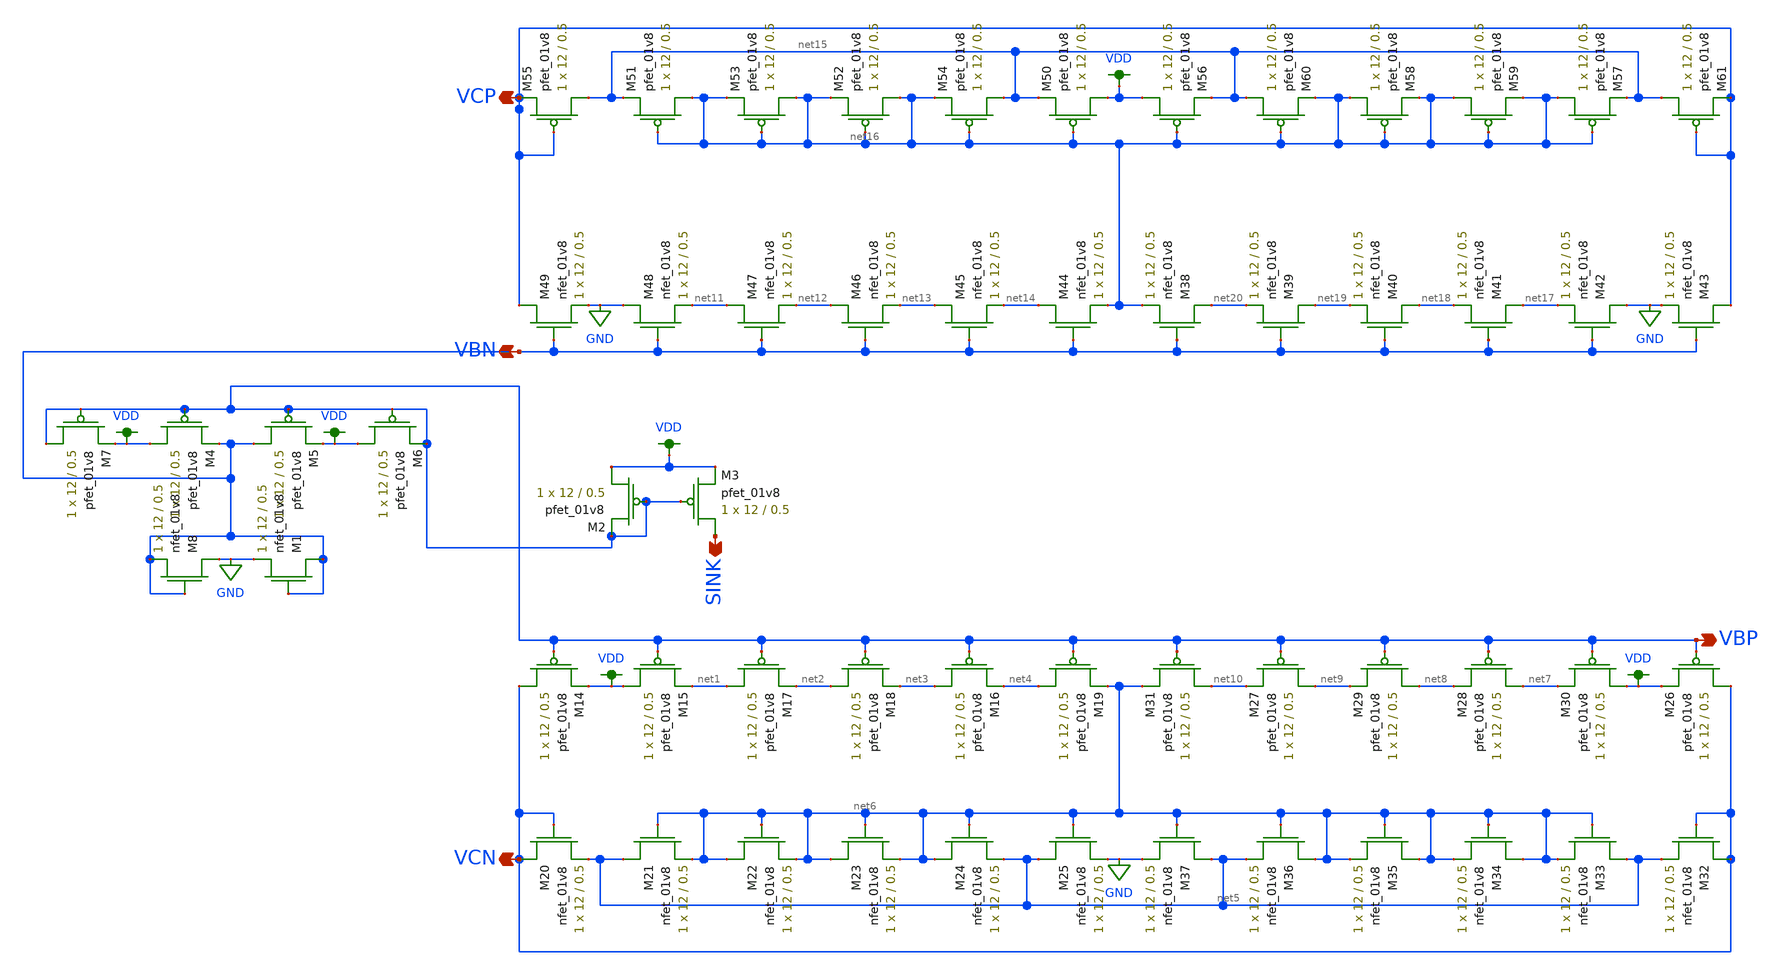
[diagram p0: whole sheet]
** sch_path: schemas/BiasGen.sch
**.subckt BiasGen VBP VCN VCP VBN SINK
*.opin VBP
*.opin VCN
*.opin VCP
*.opin VBN
*.opin SINK
XM14 VCN VBP VDD VDD sky130_fd_pr__pfet_01v8 L=0.5 W=12 nf=1 ad='int((nf+1)/2) * W/nf * 0.29' as='int((nf+2)/2) * W/nf * 0.29'
+ pd='2*int((nf+1)/2) * (W/nf + 0.29)' ps='2*int((nf+2)/2) * (W/nf + 0.29)' nrd='0.29 / W' nrs='0.29 / W'
+ sa=0 sb=0 sd=0 mult=1 m=1
XM16 net3 VBP net4 VDD sky130_fd_pr__pfet_01v8 L=0.5 W=12 nf=1 ad='int((nf+1)/2) * W/nf * 0.29' as='int((nf+2)/2) * W/nf * 0.29'
+ pd='2*int((nf+1)/2) * (W/nf + 0.29)' ps='2*int((nf+2)/2) * (W/nf + 0.29)' nrd='0.29 / W' nrs='0.29 / W'
+ sa=0 sb=0 sd=0 mult=1 m=1
XM17 net1 VBP net2 VDD sky130_fd_pr__pfet_01v8 L=0.5 W=12 nf=1 ad='int((nf+1)/2) * W/nf * 0.29' as='int((nf+2)/2) * W/nf * 0.29'
+ pd='2*int((nf+1)/2) * (W/nf + 0.29)' ps='2*int((nf+2)/2) * (W/nf + 0.29)' nrd='0.29 / W' nrs='0.29 / W'
+ sa=0 sb=0 sd=0 mult=1 m=1
XM18 net2 VBP net3 VDD sky130_fd_pr__pfet_01v8 L=0.5 W=12 nf=1 ad='int((nf+1)/2) * W/nf * 0.29' as='int((nf+2)/2) * W/nf * 0.29'
+ pd='2*int((nf+1)/2) * (W/nf + 0.29)' ps='2*int((nf+2)/2) * (W/nf + 0.29)' nrd='0.29 / W' nrs='0.29 / W'
+ sa=0 sb=0 sd=0 mult=1 m=1
XM15 VDD VBP net1 VDD sky130_fd_pr__pfet_01v8 L=0.5 W=12 nf=1 ad='int((nf+1)/2) * W/nf * 0.29' as='int((nf+2)/2) * W/nf * 0.29'
+ pd='2*int((nf+1)/2) * (W/nf + 0.29)' ps='2*int((nf+2)/2) * (W/nf + 0.29)' nrd='0.29 / W' nrs='0.29 / W'
+ sa=0 sb=0 sd=0 mult=1 m=1
XM19 net4 VBP net6 VDD sky130_fd_pr__pfet_01v8 L=0.5 W=12 nf=1 ad='int((nf+1)/2) * W/nf * 0.29' as='int((nf+2)/2) * W/nf * 0.29'
+ pd='2*int((nf+1)/2) * (W/nf + 0.29)' ps='2*int((nf+2)/2) * (W/nf + 0.29)' nrd='0.29 / W' nrs='0.29 / W'
+ sa=0 sb=0 sd=0 mult=1 m=1
XM20 VCN VCN net5 GND sky130_fd_pr__nfet_01v8 L=0.5 W=12 nf=1 ad='int((nf+1)/2) * W/nf * 0.29' as='int((nf+2)/2) * W/nf * 0.29'
+ pd='2*int((nf+1)/2) * (W/nf + 0.29)' ps='2*int((nf+2)/2) * (W/nf + 0.29)' nrd='0.29 / W' nrs='0.29 / W'
+ sa=0 sb=0 sd=0 mult=1 m=1
XM21 net5 net6 net6 GND sky130_fd_pr__nfet_01v8 L=0.5 W=12 nf=1 ad='int((nf+1)/2) * W/nf * 0.29' as='int((nf+2)/2) * W/nf * 0.29'
+ pd='2*int((nf+1)/2) * (W/nf + 0.29)' ps='2*int((nf+2)/2) * (W/nf + 0.29)' nrd='0.29 / W' nrs='0.29 / W'
+ sa=0 sb=0 sd=0 mult=1 m=1
XM22 net6 net6 net6 GND sky130_fd_pr__nfet_01v8 L=0.5 W=12 nf=1 ad='int((nf+1)/2) * W/nf * 0.29' as='int((nf+2)/2) * W/nf * 0.29'
+ pd='2*int((nf+1)/2) * (W/nf + 0.29)' ps='2*int((nf+2)/2) * (W/nf + 0.29)' nrd='0.29 / W' nrs='0.29 / W'
+ sa=0 sb=0 sd=0 mult=1 m=1
XM23 net6 net6 net6 GND sky130_fd_pr__nfet_01v8 L=0.5 W=12 nf=1 ad='int((nf+1)/2) * W/nf * 0.29' as='int((nf+2)/2) * W/nf * 0.29'
+ pd='2*int((nf+1)/2) * (W/nf + 0.29)' ps='2*int((nf+2)/2) * (W/nf + 0.29)' nrd='0.29 / W' nrs='0.29 / W'
+ sa=0 sb=0 sd=0 mult=1 m=1
XM24 net6 net6 net5 GND sky130_fd_pr__nfet_01v8 L=0.5 W=12 nf=1 ad='int((nf+1)/2) * W/nf * 0.29' as='int((nf+2)/2) * W/nf * 0.29'
+ pd='2*int((nf+1)/2) * (W/nf + 0.29)' ps='2*int((nf+2)/2) * (W/nf + 0.29)' nrd='0.29 / W' nrs='0.29 / W'
+ sa=0 sb=0 sd=0 mult=1 m=1
XM25 net5 net6 GND GND sky130_fd_pr__nfet_01v8 L=0.5 W=12 nf=1 ad='int((nf+1)/2) * W/nf * 0.29' as='int((nf+2)/2) * W/nf * 0.29'
+ pd='2*int((nf+1)/2) * (W/nf + 0.29)' ps='2*int((nf+2)/2) * (W/nf + 0.29)' nrd='0.29 / W' nrs='0.29 / W'
+ sa=0 sb=0 sd=0 mult=1 m=1
XM26 VCN VBP VDD VDD sky130_fd_pr__pfet_01v8 L=0.5 W=12 nf=1 ad='int((nf+1)/2) * W/nf * 0.29' as='int((nf+2)/2) * W/nf * 0.29'
+ pd='2*int((nf+1)/2) * (W/nf + 0.29)' ps='2*int((nf+2)/2) * (W/nf + 0.29)' nrd='0.29 / W' nrs='0.29 / W'
+ sa=0 sb=0 sd=0 mult=1 m=1
XM27 net9 VBP net10 VDD sky130_fd_pr__pfet_01v8 L=0.5 W=12 nf=1 ad='int((nf+1)/2) * W/nf * 0.29' as='int((nf+2)/2) * W/nf * 0.29'
+ pd='2*int((nf+1)/2) * (W/nf + 0.29)' ps='2*int((nf+2)/2) * (W/nf + 0.29)' nrd='0.29 / W' nrs='0.29 / W'
+ sa=0 sb=0 sd=0 mult=1 m=1
XM28 net7 VBP net8 VDD sky130_fd_pr__pfet_01v8 L=0.5 W=12 nf=1 ad='int((nf+1)/2) * W/nf * 0.29' as='int((nf+2)/2) * W/nf * 0.29'
+ pd='2*int((nf+1)/2) * (W/nf + 0.29)' ps='2*int((nf+2)/2) * (W/nf + 0.29)' nrd='0.29 / W' nrs='0.29 / W'
+ sa=0 sb=0 sd=0 mult=1 m=1
XM29 net8 VBP net9 VDD sky130_fd_pr__pfet_01v8 L=0.5 W=12 nf=1 ad='int((nf+1)/2) * W/nf * 0.29' as='int((nf+2)/2) * W/nf * 0.29'
+ pd='2*int((nf+1)/2) * (W/nf + 0.29)' ps='2*int((nf+2)/2) * (W/nf + 0.29)' nrd='0.29 / W' nrs='0.29 / W'
+ sa=0 sb=0 sd=0 mult=1 m=1
XM30 VDD VBP net7 VDD sky130_fd_pr__pfet_01v8 L=0.5 W=12 nf=1 ad='int((nf+1)/2) * W/nf * 0.29' as='int((nf+2)/2) * W/nf * 0.29'
+ pd='2*int((nf+1)/2) * (W/nf + 0.29)' ps='2*int((nf+2)/2) * (W/nf + 0.29)' nrd='0.29 / W' nrs='0.29 / W'
+ sa=0 sb=0 sd=0 mult=1 m=1
XM31 net10 VBP net6 VDD sky130_fd_pr__pfet_01v8 L=0.5 W=12 nf=1 ad='int((nf+1)/2) * W/nf * 0.29' as='int((nf+2)/2) * W/nf * 0.29'
+ pd='2*int((nf+1)/2) * (W/nf + 0.29)' ps='2*int((nf+2)/2) * (W/nf + 0.29)' nrd='0.29 / W' nrs='0.29 / W'
+ sa=0 sb=0 sd=0 mult=1 m=1
XM32 VCN VCN net5 GND sky130_fd_pr__nfet_01v8 L=0.5 W=12 nf=1 ad='int((nf+1)/2) * W/nf * 0.29' as='int((nf+2)/2) * W/nf * 0.29'
+ pd='2*int((nf+1)/2) * (W/nf + 0.29)' ps='2*int((nf+2)/2) * (W/nf + 0.29)' nrd='0.29 / W' nrs='0.29 / W'
+ sa=0 sb=0 sd=0 mult=1 m=1
XM33 net5 net6 net6 GND sky130_fd_pr__nfet_01v8 L=0.5 W=12 nf=1 ad='int((nf+1)/2) * W/nf * 0.29' as='int((nf+2)/2) * W/nf * 0.29'
+ pd='2*int((nf+1)/2) * (W/nf + 0.29)' ps='2*int((nf+2)/2) * (W/nf + 0.29)' nrd='0.29 / W' nrs='0.29 / W'
+ sa=0 sb=0 sd=0 mult=1 m=1
XM34 net6 net6 net6 GND sky130_fd_pr__nfet_01v8 L=0.5 W=12 nf=1 ad='int((nf+1)/2) * W/nf * 0.29' as='int((nf+2)/2) * W/nf * 0.29'
+ pd='2*int((nf+1)/2) * (W/nf + 0.29)' ps='2*int((nf+2)/2) * (W/nf + 0.29)' nrd='0.29 / W' nrs='0.29 / W'
+ sa=0 sb=0 sd=0 mult=1 m=1
XM35 net6 net6 net6 GND sky130_fd_pr__nfet_01v8 L=0.5 W=12 nf=1 ad='int((nf+1)/2) * W/nf * 0.29' as='int((nf+2)/2) * W/nf * 0.29'
+ pd='2*int((nf+1)/2) * (W/nf + 0.29)' ps='2*int((nf+2)/2) * (W/nf + 0.29)' nrd='0.29 / W' nrs='0.29 / W'
+ sa=0 sb=0 sd=0 mult=1 m=1
XM36 net6 net6 net5 GND sky130_fd_pr__nfet_01v8 L=0.5 W=12 nf=1 ad='int((nf+1)/2) * W/nf * 0.29' as='int((nf+2)/2) * W/nf * 0.29'
+ pd='2*int((nf+1)/2) * (W/nf + 0.29)' ps='2*int((nf+2)/2) * (W/nf + 0.29)' nrd='0.29 / W' nrs='0.29 / W'
+ sa=0 sb=0 sd=0 mult=1 m=1
XM37 net5 net6 GND GND sky130_fd_pr__nfet_01v8 L=0.5 W=12 nf=1 ad='int((nf+1)/2) * W/nf * 0.29' as='int((nf+2)/2) * W/nf * 0.29'
+ pd='2*int((nf+1)/2) * (W/nf + 0.29)' ps='2*int((nf+2)/2) * (W/nf + 0.29)' nrd='0.29 / W' nrs='0.29 / W'
+ sa=0 sb=0 sd=0 mult=1 m=1
XM44 net14 VBN net16 GND sky130_fd_pr__nfet_01v8 L=0.5 W=12 nf=1 ad='int((nf+1)/2) * W/nf * 0.29' as='int((nf+2)/2) * W/nf * 0.29'
+ pd='2*int((nf+1)/2) * (W/nf + 0.29)' ps='2*int((nf+2)/2) * (W/nf + 0.29)' nrd='0.29 / W' nrs='0.29 / W'
+ sa=0 sb=0 sd=0 mult=1 m=1
XM45 net13 VBN net14 GND sky130_fd_pr__nfet_01v8 L=0.5 W=12 nf=1 ad='int((nf+1)/2) * W/nf * 0.29' as='int((nf+2)/2) * W/nf * 0.29'
+ pd='2*int((nf+1)/2) * (W/nf + 0.29)' ps='2*int((nf+2)/2) * (W/nf + 0.29)' nrd='0.29 / W' nrs='0.29 / W'
+ sa=0 sb=0 sd=0 mult=1 m=1
XM46 net12 VBN net13 GND sky130_fd_pr__nfet_01v8 L=0.5 W=12 nf=1 ad='int((nf+1)/2) * W/nf * 0.29' as='int((nf+2)/2) * W/nf * 0.29'
+ pd='2*int((nf+1)/2) * (W/nf + 0.29)' ps='2*int((nf+2)/2) * (W/nf + 0.29)' nrd='0.29 / W' nrs='0.29 / W'
+ sa=0 sb=0 sd=0 mult=1 m=1
XM47 net11 VBN net12 GND sky130_fd_pr__nfet_01v8 L=0.5 W=12 nf=1 ad='int((nf+1)/2) * W/nf * 0.29' as='int((nf+2)/2) * W/nf * 0.29'
+ pd='2*int((nf+1)/2) * (W/nf + 0.29)' ps='2*int((nf+2)/2) * (W/nf + 0.29)' nrd='0.29 / W' nrs='0.29 / W'
+ sa=0 sb=0 sd=0 mult=1 m=1
XM48 GND VBN net11 GND sky130_fd_pr__nfet_01v8 L=0.5 W=12 nf=1 ad='int((nf+1)/2) * W/nf * 0.29' as='int((nf+2)/2) * W/nf * 0.29'
+ pd='2*int((nf+1)/2) * (W/nf + 0.29)' ps='2*int((nf+2)/2) * (W/nf + 0.29)' nrd='0.29 / W' nrs='0.29 / W'
+ sa=0 sb=0 sd=0 mult=1 m=1
XM49 VCP VBN GND GND sky130_fd_pr__nfet_01v8 L=0.5 W=12 nf=1 ad='int((nf+1)/2) * W/nf * 0.29' as='int((nf+2)/2) * W/nf * 0.29'
+ pd='2*int((nf+1)/2) * (W/nf + 0.29)' ps='2*int((nf+2)/2) * (W/nf + 0.29)' nrd='0.29 / W' nrs='0.29 / W'
+ sa=0 sb=0 sd=0 mult=1 m=1
XM50 VDD net16 net15 VDD sky130_fd_pr__pfet_01v8 L=0.5 W=12 nf=1 ad='int((nf+1)/2) * W/nf * 0.29' as='int((nf+2)/2) * W/nf * 0.29'
+ pd='2*int((nf+1)/2) * (W/nf + 0.29)' ps='2*int((nf+2)/2) * (W/nf + 0.29)' nrd='0.29 / W' nrs='0.29 / W'
+ sa=0 sb=0 sd=0 mult=1 m=1
XM51 net16 net16 net15 VDD sky130_fd_pr__pfet_01v8 L=0.5 W=12 nf=1 ad='int((nf+1)/2) * W/nf * 0.29' as='int((nf+2)/2) * W/nf * 0.29'
+ pd='2*int((nf+1)/2) * (W/nf + 0.29)' ps='2*int((nf+2)/2) * (W/nf + 0.29)' nrd='0.29 / W' nrs='0.29 / W'
+ sa=0 sb=0 sd=0 mult=1 m=1
XM52 net16 net16 net16 VDD sky130_fd_pr__pfet_01v8 L=0.5 W=12 nf=1 ad='int((nf+1)/2) * W/nf * 0.29' as='int((nf+2)/2) * W/nf * 0.29'
+ pd='2*int((nf+1)/2) * (W/nf + 0.29)' ps='2*int((nf+2)/2) * (W/nf + 0.29)' nrd='0.29 / W' nrs='0.29 / W'
+ sa=0 sb=0 sd=0 mult=1 m=1
XM53 net16 net16 net16 VDD sky130_fd_pr__pfet_01v8 L=0.5 W=12 nf=1 ad='int((nf+1)/2) * W/nf * 0.29' as='int((nf+2)/2) * W/nf * 0.29'
+ pd='2*int((nf+1)/2) * (W/nf + 0.29)' ps='2*int((nf+2)/2) * (W/nf + 0.29)' nrd='0.29 / W' nrs='0.29 / W'
+ sa=0 sb=0 sd=0 mult=1 m=1
XM54 net15 net16 net16 VDD sky130_fd_pr__pfet_01v8 L=0.5 W=12 nf=1 ad='int((nf+1)/2) * W/nf * 0.29' as='int((nf+2)/2) * W/nf * 0.29'
+ pd='2*int((nf+1)/2) * (W/nf + 0.29)' ps='2*int((nf+2)/2) * (W/nf + 0.29)' nrd='0.29 / W' nrs='0.29 / W'
+ sa=0 sb=0 sd=0 mult=1 m=1
XM55 net15 VCP VCP VDD sky130_fd_pr__pfet_01v8 L=0.5 W=12 nf=1 ad='int((nf+1)/2) * W/nf * 0.29' as='int((nf+2)/2) * W/nf * 0.29'
+ pd='2*int((nf+1)/2) * (W/nf + 0.29)' ps='2*int((nf+2)/2) * (W/nf + 0.29)' nrd='0.29 / W' nrs='0.29 / W'
+ sa=0 sb=0 sd=0 mult=1 m=1
XM38 net20 VBN net16 GND sky130_fd_pr__nfet_01v8 L=0.5 W=12 nf=1 ad='int((nf+1)/2) * W/nf * 0.29' as='int((nf+2)/2) * W/nf * 0.29'
+ pd='2*int((nf+1)/2) * (W/nf + 0.29)' ps='2*int((nf+2)/2) * (W/nf + 0.29)' nrd='0.29 / W' nrs='0.29 / W'
+ sa=0 sb=0 sd=0 mult=1 m=1
XM39 net19 VBN net20 GND sky130_fd_pr__nfet_01v8 L=0.5 W=12 nf=1 ad='int((nf+1)/2) * W/nf * 0.29' as='int((nf+2)/2) * W/nf * 0.29'
+ pd='2*int((nf+1)/2) * (W/nf + 0.29)' ps='2*int((nf+2)/2) * (W/nf + 0.29)' nrd='0.29 / W' nrs='0.29 / W'
+ sa=0 sb=0 sd=0 mult=1 m=1
XM40 net18 VBN net19 GND sky130_fd_pr__nfet_01v8 L=0.5 W=12 nf=1 ad='int((nf+1)/2) * W/nf * 0.29' as='int((nf+2)/2) * W/nf * 0.29'
+ pd='2*int((nf+1)/2) * (W/nf + 0.29)' ps='2*int((nf+2)/2) * (W/nf + 0.29)' nrd='0.29 / W' nrs='0.29 / W'
+ sa=0 sb=0 sd=0 mult=1 m=1
XM41 net17 VBN net18 GND sky130_fd_pr__nfet_01v8 L=0.5 W=12 nf=1 ad='int((nf+1)/2) * W/nf * 0.29' as='int((nf+2)/2) * W/nf * 0.29'
+ pd='2*int((nf+1)/2) * (W/nf + 0.29)' ps='2*int((nf+2)/2) * (W/nf + 0.29)' nrd='0.29 / W' nrs='0.29 / W'
+ sa=0 sb=0 sd=0 mult=1 m=1
XM42 GND VBN net17 GND sky130_fd_pr__nfet_01v8 L=0.5 W=12 nf=1 ad='int((nf+1)/2) * W/nf * 0.29' as='int((nf+2)/2) * W/nf * 0.29'
+ pd='2*int((nf+1)/2) * (W/nf + 0.29)' ps='2*int((nf+2)/2) * (W/nf + 0.29)' nrd='0.29 / W' nrs='0.29 / W'
+ sa=0 sb=0 sd=0 mult=1 m=1
XM43 VCP VBN GND GND sky130_fd_pr__nfet_01v8 L=0.5 W=12 nf=1 ad='int((nf+1)/2) * W/nf * 0.29' as='int((nf+2)/2) * W/nf * 0.29'
+ pd='2*int((nf+1)/2) * (W/nf + 0.29)' ps='2*int((nf+2)/2) * (W/nf + 0.29)' nrd='0.29 / W' nrs='0.29 / W'
+ sa=0 sb=0 sd=0 mult=1 m=1
XM56 VDD net16 net15 VDD sky130_fd_pr__pfet_01v8 L=0.5 W=12 nf=1 ad='int((nf+1)/2) * W/nf * 0.29' as='int((nf+2)/2) * W/nf * 0.29'
+ pd='2*int((nf+1)/2) * (W/nf + 0.29)' ps='2*int((nf+2)/2) * (W/nf + 0.29)' nrd='0.29 / W' nrs='0.29 / W'
+ sa=0 sb=0 sd=0 mult=1 m=1
XM57 net16 net16 net15 VDD sky130_fd_pr__pfet_01v8 L=0.5 W=12 nf=1 ad='int((nf+1)/2) * W/nf * 0.29' as='int((nf+2)/2) * W/nf * 0.29'
+ pd='2*int((nf+1)/2) * (W/nf + 0.29)' ps='2*int((nf+2)/2) * (W/nf + 0.29)' nrd='0.29 / W' nrs='0.29 / W'
+ sa=0 sb=0 sd=0 mult=1 m=1
XM58 net16 net16 net16 VDD sky130_fd_pr__pfet_01v8 L=0.5 W=12 nf=1 ad='int((nf+1)/2) * W/nf * 0.29' as='int((nf+2)/2) * W/nf * 0.29'
+ pd='2*int((nf+1)/2) * (W/nf + 0.29)' ps='2*int((nf+2)/2) * (W/nf + 0.29)' nrd='0.29 / W' nrs='0.29 / W'
+ sa=0 sb=0 sd=0 mult=1 m=1
XM59 net16 net16 net16 VDD sky130_fd_pr__pfet_01v8 L=0.5 W=12 nf=1 ad='int((nf+1)/2) * W/nf * 0.29' as='int((nf+2)/2) * W/nf * 0.29'
+ pd='2*int((nf+1)/2) * (W/nf + 0.29)' ps='2*int((nf+2)/2) * (W/nf + 0.29)' nrd='0.29 / W' nrs='0.29 / W'
+ sa=0 sb=0 sd=0 mult=1 m=1
XM60 net15 net16 net16 VDD sky130_fd_pr__pfet_01v8 L=0.5 W=12 nf=1 ad='int((nf+1)/2) * W/nf * 0.29' as='int((nf+2)/2) * W/nf * 0.29'
+ pd='2*int((nf+1)/2) * (W/nf + 0.29)' ps='2*int((nf+2)/2) * (W/nf + 0.29)' nrd='0.29 / W' nrs='0.29 / W'
+ sa=0 sb=0 sd=0 mult=1 m=1
XM61 net15 VCP VCP VDD sky130_fd_pr__pfet_01v8 L=0.5 W=12 nf=1 ad='int((nf+1)/2) * W/nf * 0.29' as='int((nf+2)/2) * W/nf * 0.29'
+ pd='2*int((nf+1)/2) * (W/nf + 0.29)' ps='2*int((nf+2)/2) * (W/nf + 0.29)' nrd='0.29 / W' nrs='0.29 / W'
+ sa=0 sb=0 sd=0 mult=1 m=1
XM4 VDD VBP VBN VDD sky130_fd_pr__pfet_01v8 L=0.5 W=12 nf=1 ad='int((nf+1)/2) * W/nf * 0.29' as='int((nf+2)/2) * W/nf * 0.29'
+ pd='2*int((nf+1)/2) * (W/nf + 0.29)' ps='2*int((nf+2)/2) * (W/nf + 0.29)' nrd='0.29 / W' nrs='0.29 / W'
+ sa=0 sb=0 sd=0 mult=1 m=1
XM5 VBN VBP VDD VDD sky130_fd_pr__pfet_01v8 L=0.5 W=12 nf=1 ad='int((nf+1)/2) * W/nf * 0.29' as='int((nf+2)/2) * W/nf * 0.29'
+ pd='2*int((nf+1)/2) * (W/nf + 0.29)' ps='2*int((nf+2)/2) * (W/nf + 0.29)' nrd='0.29 / W' nrs='0.29 / W'
+ sa=0 sb=0 sd=0 mult=1 m=1
XM6 VDD VBP VBP VDD sky130_fd_pr__pfet_01v8 L=0.5 W=12 nf=1 ad='int((nf+1)/2) * W/nf * 0.29' as='int((nf+2)/2) * W/nf * 0.29'
+ pd='2*int((nf+1)/2) * (W/nf + 0.29)' ps='2*int((nf+2)/2) * (W/nf + 0.29)' nrd='0.29 / W' nrs='0.29 / W'
+ sa=0 sb=0 sd=0 mult=1 m=1
XM7 VBP VBP VDD VDD sky130_fd_pr__pfet_01v8 L=0.5 W=12 nf=1 ad='int((nf+1)/2) * W/nf * 0.29' as='int((nf+2)/2) * W/nf * 0.29'
+ pd='2*int((nf+1)/2) * (W/nf + 0.29)' ps='2*int((nf+2)/2) * (W/nf + 0.29)' nrd='0.29 / W' nrs='0.29 / W'
+ sa=0 sb=0 sd=0 mult=1 m=1
XM1 VBN VBN GND GND sky130_fd_pr__nfet_01v8 L=0.5 W=12 nf=1 ad='int((nf+1)/2) * W/nf * 0.29' as='int((nf+2)/2) * W/nf * 0.29'
+ pd='2*int((nf+1)/2) * (W/nf + 0.29)' ps='2*int((nf+2)/2) * (W/nf + 0.29)' nrd='0.29 / W' nrs='0.29 / W'
+ sa=0 sb=0 sd=0 mult=1 m=1
XM8 GND VBN VBN GND sky130_fd_pr__nfet_01v8 L=0.5 W=12 nf=1 ad='int((nf+1)/2) * W/nf * 0.29' as='int((nf+2)/2) * W/nf * 0.29'
+ pd='2*int((nf+1)/2) * (W/nf + 0.29)' ps='2*int((nf+2)/2) * (W/nf + 0.29)' nrd='0.29 / W' nrs='0.29 / W'
+ sa=0 sb=0 sd=0 mult=1 m=1
XM2 VDD VBP VBP VDD sky130_fd_pr__pfet_01v8 L=0.5 W=12 nf=1 ad='int((nf+1)/2) * W/nf * 0.29' as='int((nf+2)/2) * W/nf * 0.29'
+ pd='2*int((nf+1)/2) * (W/nf + 0.29)' ps='2*int((nf+2)/2) * (W/nf + 0.29)' nrd='0.29 / W' nrs='0.29 / W'
+ sa=0 sb=0 sd=0 mult=1 m=1
XM3 SINK VBP VDD VDD sky130_fd_pr__pfet_01v8 L=0.5 W=12 nf=1 ad='int((nf+1)/2) * W/nf * 0.29' as='int((nf+2)/2) * W/nf * 0.29'
+ pd='2*int((nf+1)/2) * (W/nf + 0.29)' ps='2*int((nf+2)/2) * (W/nf + 0.29)' nrd='0.29 / W' nrs='0.29 / W'
+ sa=0 sb=0 sd=0 mult=1 m=1
**.ends
.GLOBAL VDD
.GLOBAL GND
.end
